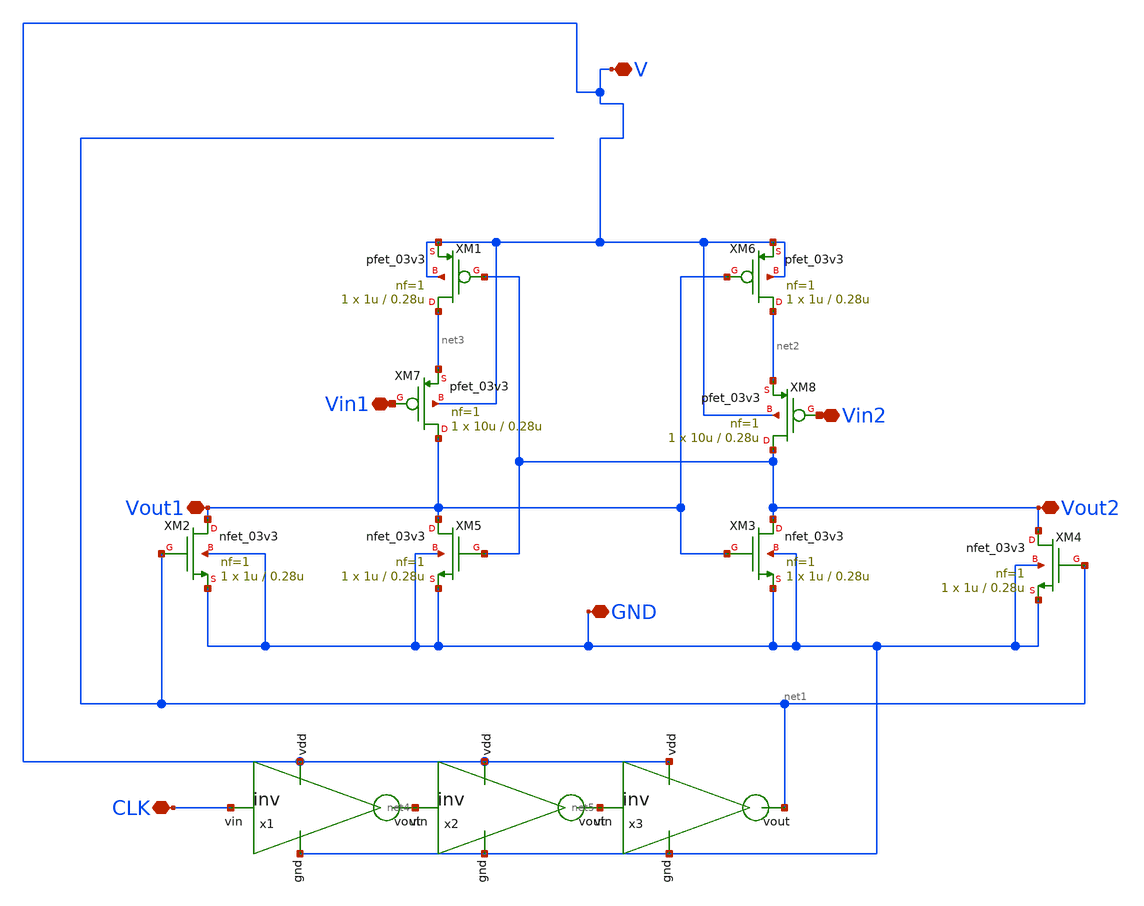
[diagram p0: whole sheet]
** sch_path: xschem/designs/strongarm.sch
**.subckt strongarm V Vout1 Vin1 Vin2 Vout2 CLK GND
*.iopin V
*.iopin Vout1
*.iopin Vin1
*.iopin Vin2
*.iopin Vout2
*.iopin CLK
*.iopin GND
XM1 net3 Vout2 V V pfet_03v3 L=0.28u W=1u nf=1 ad='int((nf+1)/2) * W/nf * 0.18u' as='int((nf+2)/2) * W/nf * 0.18u'
+ pd='2*int((nf+1)/2) * (W/nf + 0.18u)' ps='2*int((nf+2)/2) * (W/nf + 0.18u)' nrd='0.18u / W' nrs='0.18u / W'
+ sa=0 sb=0 sd=0 m=1
XM2 Vout1 net1 GND GND nfet_03v3 L=0.28u W=1u nf=1 ad='int((nf+1)/2) * W/nf * 0.18u' as='int((nf+2)/2) * W/nf * 0.18u'
+ pd='2*int((nf+1)/2) * (W/nf + 0.18u)' ps='2*int((nf+2)/2) * (W/nf + 0.18u)' nrd='0.18u / W' nrs='0.18u / W'
+ sa=0 sb=0 sd=0 m=1
XM3 Vout2 Vout1 GND GND nfet_03v3 L=0.28u W=1u nf=1 ad='int((nf+1)/2) * W/nf * 0.18u' as='int((nf+2)/2) * W/nf * 0.18u'
+ pd='2*int((nf+1)/2) * (W/nf + 0.18u)' ps='2*int((nf+2)/2) * (W/nf + 0.18u)' nrd='0.18u / W' nrs='0.18u / W'
+ sa=0 sb=0 sd=0 m=1
XM4 Vout2 net1 GND GND nfet_03v3 L=0.28u W=1u nf=1 ad='int((nf+1)/2) * W/nf * 0.18u' as='int((nf+2)/2) * W/nf * 0.18u'
+ pd='2*int((nf+1)/2) * (W/nf + 0.18u)' ps='2*int((nf+2)/2) * (W/nf + 0.18u)' nrd='0.18u / W' nrs='0.18u / W'
+ sa=0 sb=0 sd=0 m=1
XM5 Vout1 Vout2 GND GND nfet_03v3 L=0.28u W=1u nf=1 ad='int((nf+1)/2) * W/nf * 0.18u' as='int((nf+2)/2) * W/nf * 0.18u'
+ pd='2*int((nf+1)/2) * (W/nf + 0.18u)' ps='2*int((nf+2)/2) * (W/nf + 0.18u)' nrd='0.18u / W' nrs='0.18u / W'
+ sa=0 sb=0 sd=0 m=1
XM6 net2 Vout1 V V pfet_03v3 L=0.28u W=1u nf=1 ad='int((nf+1)/2) * W/nf * 0.18u' as='int((nf+2)/2) * W/nf * 0.18u'
+ pd='2*int((nf+1)/2) * (W/nf + 0.18u)' ps='2*int((nf+2)/2) * (W/nf + 0.18u)' nrd='0.18u / W' nrs='0.18u / W'
+ sa=0 sb=0 sd=0 m=1
XM7 Vout1 Vin1 net3 V pfet_03v3 L=0.28u W=10u nf=1 ad='int((nf+1)/2) * W/nf * 0.18u' as='int((nf+2)/2) * W/nf * 0.18u'
+ pd='2*int((nf+1)/2) * (W/nf + 0.18u)' ps='2*int((nf+2)/2) * (W/nf + 0.18u)' nrd='0.18u / W' nrs='0.18u / W'
+ sa=0 sb=0 sd=0 m=1
XM8 Vout2 Vin2 net2 V pfet_03v3 L=0.28u W=10u nf=1 ad='int((nf+1)/2) * W/nf * 0.18u' as='int((nf+2)/2) * W/nf * 0.18u'
+ pd='2*int((nf+1)/2) * (W/nf + 0.18u)' ps='2*int((nf+2)/2) * (W/nf + 0.18u)' nrd='0.18u / W' nrs='0.18u / W'
+ sa=0 sb=0 sd=0 m=1
x1 V GND net4 CLK inv cl=0.28u wp=0.44u wn=0.22u wx=.22u mx=1
x2 V GND net5 net4 inv cl=0.28u wp=0.44u wn=0.22u wx=10u mx=1
x3 V GND net1 net5 inv cl=0.28u wp=0.44u wn=0.22u wx=10u mx=1
**.ends

* expanding   symbol:  inv.sym # of pins=4
** sym_path: xschem/designs/inv.sym
** sch_path: xschem/designs/inv.sch
.subckt inv vdd gnd vout vin  cl=0.28u wp=0.44u wn=0.22u wx=0.22u mx=1
*.ipin gnd
*.ipin vdd
*.ipin vin
*.opin vout
XM1 gnd vin vout gnd nfet_03v3 L=0.28u W=Wx nf=1 ad='int((nf+1)/2) * W/nf * 0.18u' as='int((nf+2)/2) * W/nf * 0.18u'
+ pd='2*int((nf+1)/2) * (W/nf + 0.18u)' ps='2*int((nf+2)/2) * (W/nf + 0.18u)' nrd='0.18u / W' nrs='0.18u / W'
+ sa=0 sb=0 sd=0 m=1
XM2 vdd vin vout vdd pfet_03v3 L=0.28u W=Wx nf=1 ad='int((nf+1)/2) * W/nf * 0.18u' as='int((nf+2)/2) * W/nf * 0.18u'
+ pd='2*int((nf+1)/2) * (W/nf + 0.18u)' ps='2*int((nf+2)/2) * (W/nf + 0.18u)' nrd='0.18u / W' nrs='0.18u / W'
+ sa=0 sb=0 sd=0 m=1
.ends

.end
